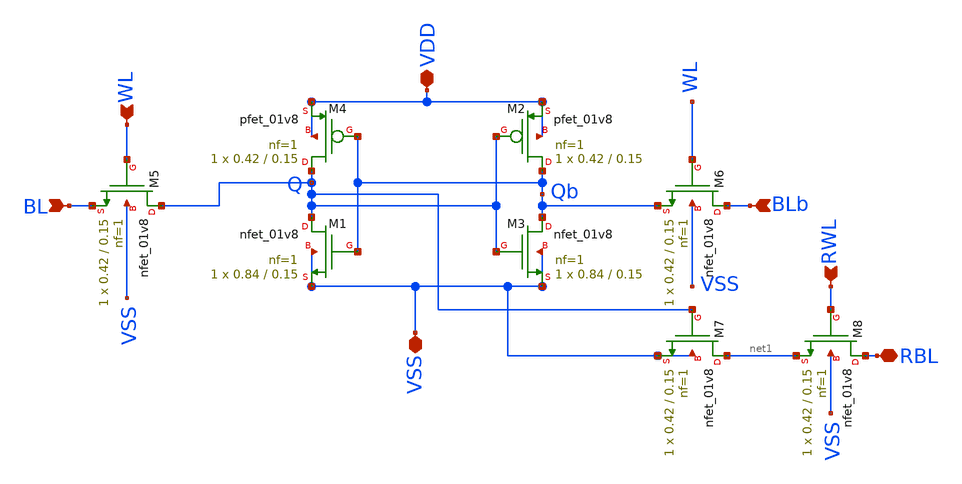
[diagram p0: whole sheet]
** sch_path: schematics/sram_8t_bitcell.sch
**.subckt sram_8t_bitcell VDD WL BL RWL BLb RBL VSS
*.iopin VDD
*.ipin WL
*.ipin BL
*.ipin RWL
*.ipin BLb
*.iopin RBL
*.iopin VSS
XM3 Qb Q VSS VSS sky130_fd_pr__nfet_01v8 L=0.15 W=0.84 nf=1 ad='int((1 + 1)/2) * 0.84 / 1 * 0.29' as='int((1 + 2)/2) * 0.84 / 1 * 0.29'
+ pd='2*int((1 + 1)/2) * (0.84 / 1 + 0.29)' ps='2*int((1 + 2)/2) * (0.84 / 1 + 0.29)' nrd='0.29 / 0.84 '
+ nrs='0.29 / 0.84 ' sa=0 sb=0 sd=0 mult=1 m=1
XM1 Q Qb VSS VSS sky130_fd_pr__nfet_01v8 L=0.15 W=0.84 nf=1 ad='int((1 + 1)/2) * 0.84 / 1 * 0.29' as='int((1 + 2)/2) * 0.84 / 1 * 0.29'
+ pd='2*int((1 + 1)/2) * (0.84 / 1 + 0.29)' ps='2*int((1 + 2)/2) * (0.84 / 1 + 0.29)' nrd='0.29 / 0.84 '
+ nrs='0.29 / 0.84 ' sa=0 sb=0 sd=0 mult=1 m=1
XM2 Qb Q VDD VDD sky130_fd_pr__pfet_01v8 L=0.15 W=0.42 nf=1 ad='int((1 + 1)/2) * 0.42 / 1 * 0.29' as='int((1 + 2)/2) * 0.42 / 1 * 0.29'
+ pd='2*int((1 + 1)/2) * (0.42 / 1 + 0.29)' ps='2*int((1 + 2)/2) * (0.42 / 1 + 0.29)' nrd='0.29 / 0.42 '
+ nrs='0.29 / 0.42 ' sa=0 sb=0 sd=0 mult=1 m=1
XM4 Q Qb VDD VDD sky130_fd_pr__pfet_01v8 L=0.15 W=0.42 nf=1 ad='int((1 + 1)/2) * 0.42 / 1 * 0.29' as='int((1 + 2)/2) * 0.42 / 1 * 0.29'
+ pd='2*int((1 + 1)/2) * (0.42 / 1 + 0.29)' ps='2*int((1 + 2)/2) * (0.42 / 1 + 0.29)' nrd='0.29 / 0.42 '
+ nrs='0.29 / 0.42 ' sa=0 sb=0 sd=0 mult=1 m=1
XM5 Q WL BL VSS sky130_fd_pr__nfet_01v8 L=0.15 W=0.42 nf=1 ad='int((1 + 1)/2) * 0.42 / 1 * 0.29' as='int((1 + 2)/2) * 0.42 / 1 * 0.29'
+ pd='2*int((1 + 1)/2) * (0.42 / 1 + 0.29)' ps='2*int((1 + 2)/2) * (0.42 / 1 + 0.29)' nrd='0.29 / 0.42 '
+ nrs='0.29 / 0.42 ' sa=0 sb=0 sd=0 mult=1 m=1
XM6 BLb WL Qb VSS sky130_fd_pr__nfet_01v8 L=0.15 W=0.42 nf=1 ad='int((1 + 1)/2) * 0.42 / 1 * 0.29' as='int((1 + 2)/2) * 0.42 / 1 * 0.29'
+ pd='2*int((1 + 1)/2) * (0.42 / 1 + 0.29)' ps='2*int((1 + 2)/2) * (0.42 / 1 + 0.29)' nrd='0.29 / 0.42 '
+ nrs='0.29 / 0.42 ' sa=0 sb=0 sd=0 mult=1 m=1
XM7 net1 Q VSS VSS sky130_fd_pr__nfet_01v8 L=0.15 W=0.42 nf=1 ad='int((1 + 1)/2) * 0.42 / 1 * 0.29' as='int((1 + 2)/2) * 0.42 / 1 * 0.29'
+ pd='2*int((1 + 1)/2) * (0.42 / 1 + 0.29)' ps='2*int((1 + 2)/2) * (0.42 / 1 + 0.29)' nrd='0.29 / 0.42 '
+ nrs='0.29 / 0.42 ' sa=0 sb=0 sd=0 mult=1 m=1
XM8 RBL RWL net1 VSS sky130_fd_pr__nfet_01v8 L=0.15 W=0.42 nf=1 ad='int((1 + 1)/2) * 0.42 / 1 * 0.29'
+ as='int((1 + 2)/2) * 0.42 / 1 * 0.29' pd='2*int((1 + 1)/2) * (0.42 / 1 + 0.29)' ps='2*int((1 + 2)/2) * (0.42 / 1 + 0.29)'
+ nrd='0.29 / 0.42 ' nrs='0.29 / 0.42 ' sa=0 sb=0 sd=0 mult=1 m=1
**.ends
.end
